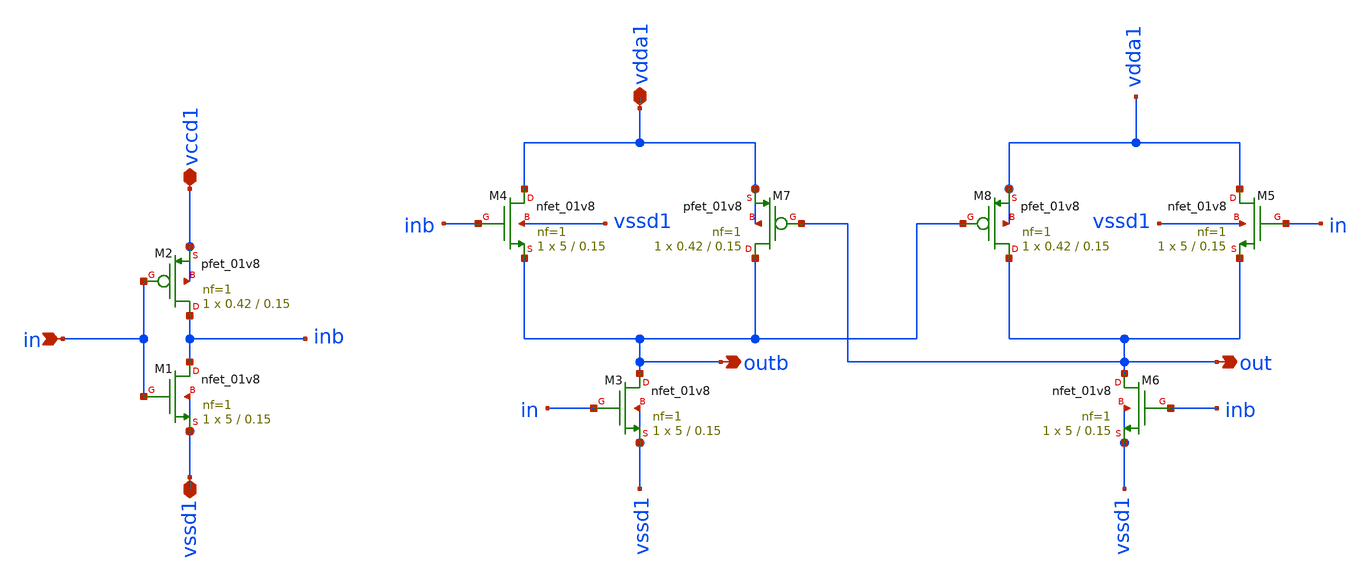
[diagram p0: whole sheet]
** sch_path: xschem/tryandtest/level_up_shifter.sch
**.subckt level_up_shifter in vccd1 vssd1 vdda1 out outb
*.ipin in
*.iopin vccd1
*.iopin vssd1
*.iopin vdda1
*.opin out
*.opin outb
XM1 inb in vssd1 vssd1 sky130_fd_pr__nfet_01v8 L=0.15 W=5 nf=1 ad='int((nf+1)/2) * W/nf * 0.29' as='int((nf+2)/2) * W/nf * 0.29'
+ pd='2*int((nf+1)/2) * (W/nf + 0.29)' ps='2*int((nf+2)/2) * (W/nf + 0.29)' nrd='0.29 / W' nrs='0.29 / W'
+ sa=0 sb=0 sd=0 mult=1 m=1
XM2 inb in vccd1 vccd1 sky130_fd_pr__pfet_01v8 L=0.15 W=0.42 nf=1 ad='int((nf+1)/2) * W/nf * 0.29' as='int((nf+2)/2) * W/nf * 0.29'
+ pd='2*int((nf+1)/2) * (W/nf + 0.29)' ps='2*int((nf+2)/2) * (W/nf + 0.29)' nrd='0.29 / W' nrs='0.29 / W'
+ sa=0 sb=0 sd=0 mult=1 m=1
XM4 vdda1 inb outb vssd1 sky130_fd_pr__nfet_01v8 L=0.15 W=5 nf=1 ad='int((nf+1)/2) * W/nf * 0.29' as='int((nf+2)/2) * W/nf * 0.29'
+ pd='2*int((nf+1)/2) * (W/nf + 0.29)' ps='2*int((nf+2)/2) * (W/nf + 0.29)' nrd='0.29 / W' nrs='0.29 / W'
+ sa=0 sb=0 sd=0 mult=1 m=1
XM5 vdda1 in out vssd1 sky130_fd_pr__nfet_01v8 L=0.15 W=5 nf=1 ad='int((nf+1)/2) * W/nf * 0.29' as='int((nf+2)/2) * W/nf * 0.29'
+ pd='2*int((nf+1)/2) * (W/nf + 0.29)' ps='2*int((nf+2)/2) * (W/nf + 0.29)' nrd='0.29 / W' nrs='0.29 / W'
+ sa=0 sb=0 sd=0 mult=1 m=1
XM7 outb out vdda1 vdda1 sky130_fd_pr__pfet_01v8 L=0.15 W=0.42 nf=1 ad='int((nf+1)/2) * W/nf * 0.29'
+ as='int((nf+2)/2) * W/nf * 0.29' pd='2*int((nf+1)/2) * (W/nf + 0.29)' ps='2*int((nf+2)/2) * (W/nf + 0.29)'
+ nrd='0.29 / W' nrs='0.29 / W' sa=0 sb=0 sd=0 mult=1 m=1
XM8 out outb vdda1 vdda1 sky130_fd_pr__pfet_01v8 L=0.15 W=0.42 nf=1 ad='int((nf+1)/2) * W/nf * 0.29'
+ as='int((nf+2)/2) * W/nf * 0.29' pd='2*int((nf+1)/2) * (W/nf + 0.29)' ps='2*int((nf+2)/2) * (W/nf + 0.29)'
+ nrd='0.29 / W' nrs='0.29 / W' sa=0 sb=0 sd=0 mult=1 m=1
XM3 outb in vssd1 vssd1 sky130_fd_pr__nfet_01v8 L=0.15 W=5 nf=1 ad='int((nf+1)/2) * W/nf * 0.29' as='int((nf+2)/2) * W/nf * 0.29'
+ pd='2*int((nf+1)/2) * (W/nf + 0.29)' ps='2*int((nf+2)/2) * (W/nf + 0.29)' nrd='0.29 / W' nrs='0.29 / W'
+ sa=0 sb=0 sd=0 mult=1 m=1
XM6 out inb vssd1 vssd1 sky130_fd_pr__nfet_01v8 L=0.15 W=5 nf=1 ad='int((nf+1)/2) * W/nf * 0.29' as='int((nf+2)/2) * W/nf * 0.29'
+ pd='2*int((nf+1)/2) * (W/nf + 0.29)' ps='2*int((nf+2)/2) * (W/nf + 0.29)' nrd='0.29 / W' nrs='0.29 / W'
+ sa=0 sb=0 sd=0 mult=1 m=1
**.ends
.end
